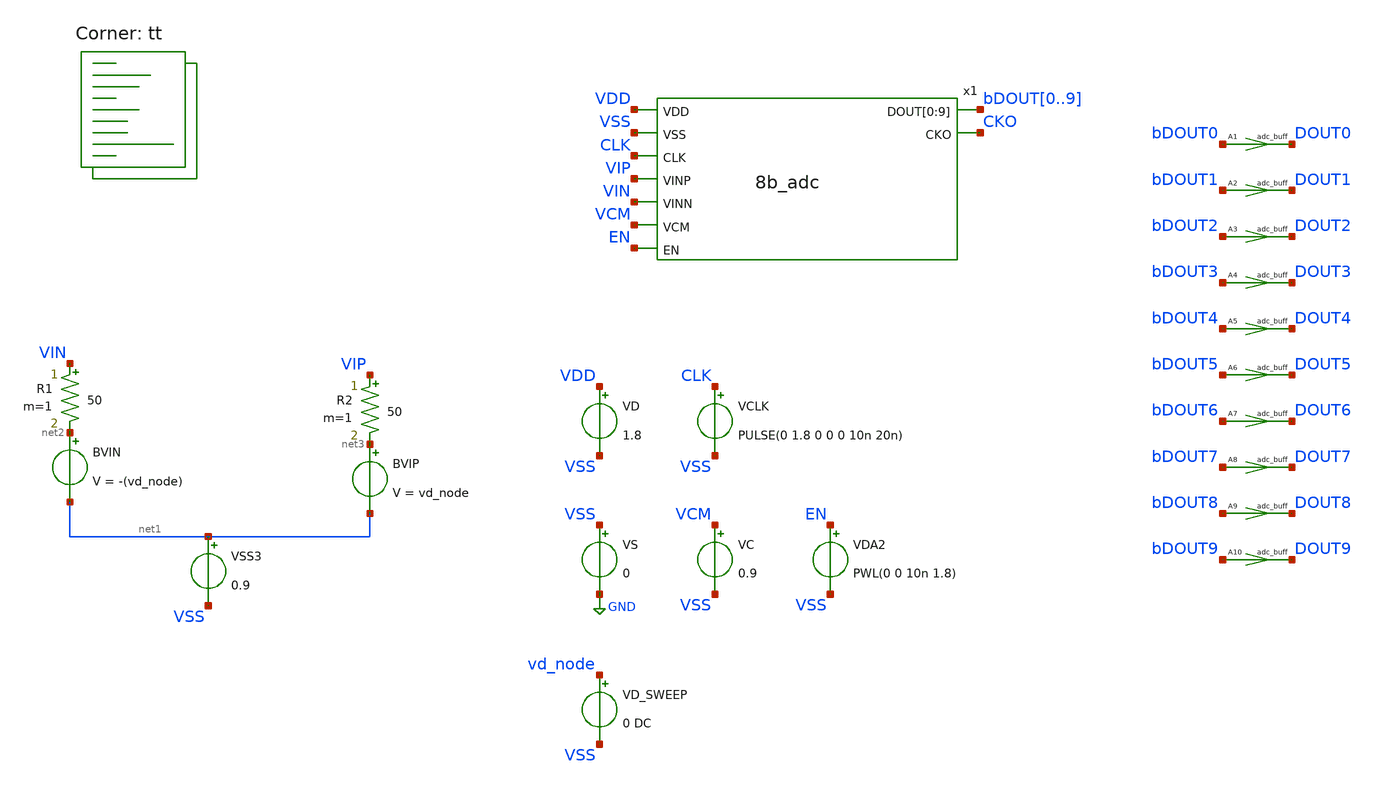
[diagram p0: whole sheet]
** sch_path: xschem/adc_dc_sim.sch
**.subckt adc_dc_sim
BVIN net2 net1 V = -(vd_node)
BVIP net3 net1 V = vd_node
VSS3 net1 VSS 0.9
R1 VIN net2 50 m=1
R2 VIP net3 50 m=1
VS VSS GND 0
VD VDD VSS 1.8
VCLK CLK VSS PULSE(0 1.8 0 0 0 10n 20n)
x1 VDD VSS CLK VIP VIN VCM EN bDOUT0 bDOUT1 bDOUT2 bDOUT3 bDOUT4 bDOUT5 bDOUT6 bDOUT7 bDOUT8 bDOUT9
+ CKO 8b_adc
VC VCM VSS 0.9
VDA2 EN VSS PWL(0 0 10n 1.8)
A1 [ bDOUT0 ] [ DOUT0 ] adc_buff
A2 [ bDOUT1 ] [ DOUT1 ] adc_buff
A3 [ bDOUT2 ] [ DOUT2 ] adc_buff
A4 [ bDOUT3 ] [ DOUT3 ] adc_buff
A5 [ bDOUT4 ] [ DOUT4 ] adc_buff
A6 [ bDOUT5 ] [ DOUT5 ] adc_buff
A7 [ bDOUT6 ] [ DOUT6 ] adc_buff
A8 [ bDOUT7 ] [ DOUT7 ] adc_buff
A9 [ bDOUT8 ] [ DOUT8 ] adc_buff
A10 [ bDOUT9 ] [ DOUT9 ] adc_buff
VD_SWEEP vd_node VSS 0 DC
**** begin user architecture code

** opencircuitdesign pdks install
* .lib $::SKYWATER_MODELS/sky130.lib.spice tt
*.include $PDK_ROOT/$PDK/libs.ref/sky130_fd_sc_hdll/spice/sky130_fd_sc_hdll.spice
.include $PDK_ROOT/$PDK/libs.ref/sky130_fd_sc_hs/spice/sky130_fd_sc_hs.spice
*.include $PDK_ROOT/$PDK/libs.ref/sky130_fd_sc_hd/spice/sky130_fd_sc_hd.spice



.option wnflag=0 bypass=1
.options method=trap rawfile=binary
.options solver=klu nomod
Eout out 0 VALUE = { ((V(dout0)*512 + V(dout1)*256 + V(dout2)*128 + V(dout3)*64 + V(dout4)*32 + V(dout5)*16 + V(dout6)*8 + V(dout7)*4 + V(dout8)*2 + V(dout9)*1)/3.3) - 512 }
Epow pow 0 VALUE = { V(vdd)*(-i(vd)) }

.model adc_buff adc_bridge(in_low=0.18 in_high=1.62 rise_delay=100p fall_delay=100p)
.control
global netlist_dir .
set num_threads=16
save cko out pow vip vin x1.vcp x1.vcn
let V_in_start = -0.9     ; Tegangan input DC awal (misal, 0V)
let V_in_stop = 0.9       ; Tegangan input DC akhir (misal, VREF atau VDD)
let V_in_step = 0.00017 ; Langkah tegangan DC (harus sangat kecil, < 0.1 LSB idealnya)

echo "Memulai DC Sweep untuk analisis statik ADC..."
dc VD_SWEEP V_in_start V_in_stop V_in_step

echo "Simulasi DC selesai."

rusage dciter dcsolvetime
meas tran inst_pow MAX pow from=1n to=535u
meas tran avg_pow  AVG pow from=1n to=535u
remzerovec
write adc10b_tb_static.raw
wrdata adc10b_tb_static.txt out cko pow
quit 1
.endc


.lib $::SKYWATER_MODELS/sky130.lib.spice tt
**** end user architecture code
**.ends
.GLOBAL GND
.end
